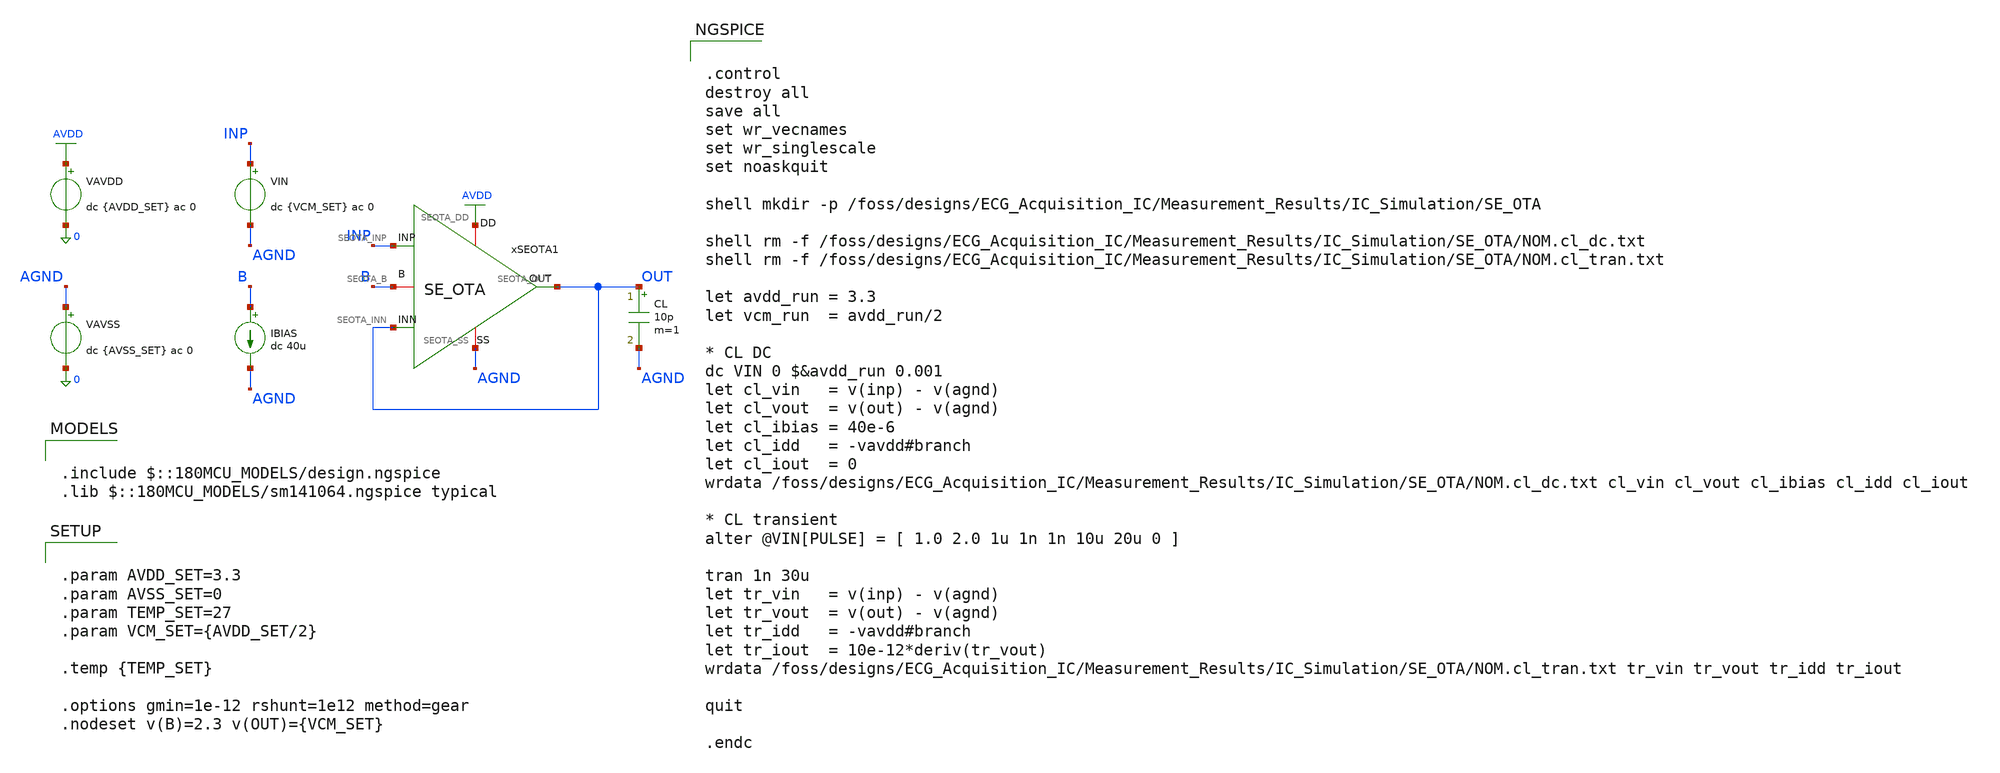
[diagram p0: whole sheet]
** sch_path: Design_Files/IC Design/Testbench/SE_OTA_OTA/Close_Loop/SE_OTA_TB_CL_NOM.sch
**.subckt SE_OTA_TB_CL_NOM
CL OUT AGND 10p m=1
xSEOTA1 AVDD AGND INP OUT OUT B SE_OTA
IBIAS B AGND dc 40u
VAVDD AVDD 0 dc {AVDD_SET} ac 0
.save i(vavdd)
VIN INP AGND dc {VCM_SET} ac 0
VAVSS AGND 0 dc {AVSS_SET} ac 0
.save i(vavss)
**** begin user architecture code

.include $::180MCU_MODELS/design.ngspice
.lib $::180MCU_MODELS/sm141064.ngspice typical



.control
destroy all
save all
set wr_vecnames
set wr_singlescale
set noaskquit

shell mkdir -p /foss/designs/ECG_Acquisition_IC/Measurement_Results/IC_Simulation/SE_OTA

shell rm -f /foss/designs/ECG_Acquisition_IC/Measurement_Results/IC_Simulation/SE_OTA/NOM.cl_dc.txt
shell rm -f
+ /foss/designs/ECG_Acquisition_IC/Measurement_Results/IC_Simulation/SE_OTA/NOM.cl_tran.txt

let avdd_run = 3.3
let vcm_run  = avdd_run/2

* CL DC
dc VIN 0 $&avdd_run 0.001
let cl_vin   = v(inp) - v(agnd)
let cl_vout  = v(out) - v(agnd)
let cl_ibias = 40e-6
let cl_idd   = -vavdd#branch
let cl_iout  = 0
wrdata /foss/designs/ECG_Acquisition_IC/Measurement_Results/IC_Simulation/SE_OTA/NOM.cl_dc.txt
+ cl_vin cl_vout cl_ibias cl_idd cl_iout

* CL transient
alter @VIN[PULSE] = [ 1.0 2.0 1u 1n 1n 10u 20u 0 ]

tran 1n 30u
let tr_vin   = v(inp) - v(agnd)
let tr_vout  = v(out) - v(agnd)
let tr_idd   = -vavdd#branch
let tr_iout  = 10e-12*deriv(tr_vout)
wrdata /foss/designs/ECG_Acquisition_IC/Measurement_Results/IC_Simulation/SE_OTA/NOM.cl_tran.txt
+ tr_vin tr_vout tr_idd tr_iout

quit

.endc




.param AVDD_SET=3.3
.param AVSS_SET=0
.param TEMP_SET=27
.param VCM_SET={AVDD_SET/2}

.temp {TEMP_SET}

.options gmin=1e-12 rshunt=1e12 method=gear
.nodeset v(B)=2.3 v(OUT)={VCM_SET}


**** end user architecture code
**.ends

* expanding   symbol:  ECG_Acquisition_IC/Design_Files/IC Design/Schematic/SE_OTA/SE_OTA.sym # of
*+ pins=6
** sym_path: Design_Files/IC Design/Schematic/SE_OTA/SE_OTA.sym
** sch_path: Design_Files/IC Design/Schematic/SE_OTA/SE_OTA.sch
.subckt SE_OTA SEOTA_DD SEOTA_SS SEOTA_INP SEOTA_INN SEOTA_OUT SEOTA_B
*.iopin SEOTA_DD
*.iopin SEOTA_SS
*.ipin SEOTA_INP
*.ipin SEOTA_INN
*.opin SEOTA_OUT
*.iopin SEOTA_B
XM4 net1 net4 SEOTA_SS SEOTA_SS nfet_03v3 L=2u W=2u nf=1 ad='int((nf+1)/2) * W/nf * 0.18u' as='int((nf+2)/2) * W/nf * 0.18u'
+ pd='2*int((nf+1)/2) * (W/nf + 0.18u)' ps='2*int((nf+2)/2) * (W/nf + 0.18u)' nrd='0.18u / W' nrs='0.18u / W'
+ sa=0 sb=0 sd=0 m=2
XM3 net4 net4 SEOTA_SS SEOTA_SS nfet_03v3 L=2u W=2u nf=1 ad='int((nf+1)/2) * W/nf * 0.18u' as='int((nf+2)/2) * W/nf * 0.18u'
+ pd='2*int((nf+1)/2) * (W/nf + 0.18u)' ps='2*int((nf+2)/2) * (W/nf + 0.18u)' nrd='0.18u / W' nrs='0.18u / W'
+ sa=0 sb=0 sd=0 m=2
XM1 net4 SEOTA_INN net3 SEOTA_DD pfet_03v3 L=1u W=32u nf=16 ad='int((nf+1)/2) * W/nf * 0.18u' as='int((nf+2)/2) * W/nf * 0.18u'
+ pd='2*int((nf+1)/2) * (W/nf + 0.18u)' ps='2*int((nf+2)/2) * (W/nf + 0.18u)' nrd='0.18u / W' nrs='0.18u / W'
+ sa=0 sb=0 sd=0 m=2
XM2 net1 SEOTA_INP net3 SEOTA_DD pfet_03v3 L=1u W=32u nf=16 ad='int((nf+1)/2) * W/nf * 0.18u' as='int((nf+2)/2) * W/nf * 0.18u'
+ pd='2*int((nf+1)/2) * (W/nf + 0.18u)' ps='2*int((nf+2)/2) * (W/nf + 0.18u)' nrd='0.18u / W' nrs='0.18u / W'
+ sa=0 sb=0 sd=0 m=2
XM7 SEOTA_OUT SEOTA_B SEOTA_DD SEOTA_DD pfet_03v3 L=0.5u W=56u nf=28 ad='int((nf+1)/2) * W/nf * 0.18u'
+ as='int((nf+2)/2) * W/nf * 0.18u' pd='2*int((nf+1)/2) * (W/nf + 0.18u)' ps='2*int((nf+2)/2) * (W/nf + 0.18u)'
+ nrd='0.18u / W' nrs='0.18u / W' sa=0 sb=0 sd=0 m=2
Rz net1 net2 0.5k m=1
XM5 net3 SEOTA_B SEOTA_DD SEOTA_DD pfet_03v3 L=2u W=20u nf=10 ad='int((nf+1)/2) * W/nf * 0.18u' as='int((nf+2)/2) * W/nf * 0.18u'
+ pd='2*int((nf+1)/2) * (W/nf + 0.18u)' ps='2*int((nf+2)/2) * (W/nf + 0.18u)' nrd='0.18u / W' nrs='0.18u / W'
+ sa=0 sb=0 sd=0 m=2
XM6 SEOTA_OUT net1 SEOTA_SS SEOTA_SS nfet_03v3 L=0.5u W=16u nf=8 ad='int((nf+1)/2) * W/nf * 0.18u' as='int((nf+2)/2) * W/nf * 0.18u'
+ pd='2*int((nf+1)/2) * (W/nf + 0.18u)' ps='2*int((nf+2)/2) * (W/nf + 0.18u)' nrd='0.18u / W' nrs='0.18u / W'
+ sa=0 sb=0 sd=0 m=2
XM8 SEOTA_B SEOTA_B SEOTA_DD SEOTA_DD pfet_03v3 L=2u W=50u nf=25 ad='int((nf+1)/2) * W/nf * 0.18u' as='int((nf+2)/2) * W/nf * 0.18u'
+ pd='2*int((nf+1)/2) * (W/nf + 0.18u)' ps='2*int((nf+2)/2) * (W/nf + 0.18u)' nrd='0.18u / W' nrs='0.18u / W'
+ sa=0 sb=0 sd=0 m=2
Cc net2 SEOTA_OUT 2p m=1
.ends

.GLOBAL AVDD
.end
